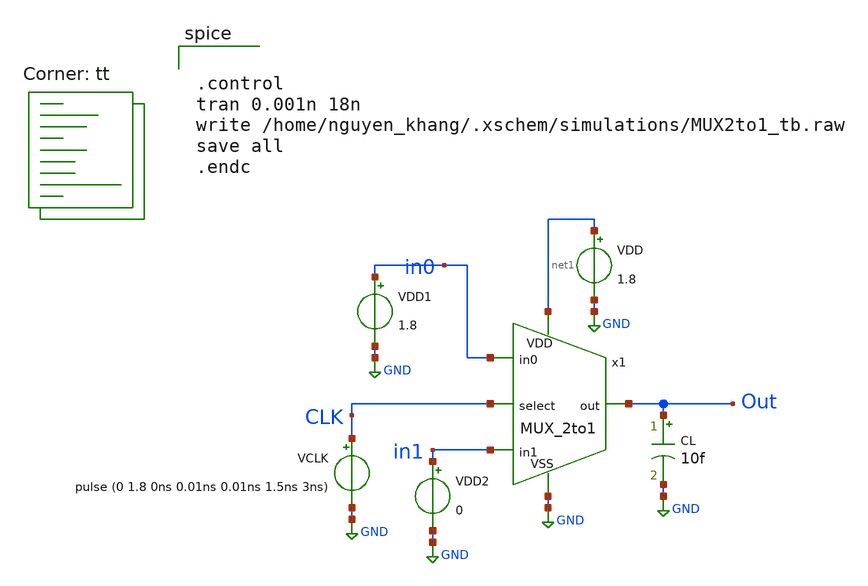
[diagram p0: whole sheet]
** sch_path: MUX_2to1_tb.sch
**.subckt MUX_2to1_tb
x1 in1 net1 Out CLK GND in0 MUX_2to1
VCLK CLK GND pulse (0 1.8 0ns 0.01ns 0.01ns 1.5ns 3ns)
VDD net1 GND 1.8
CL Out GND 10f m=1
VDD1 in0 GND 1.8
VDD2 in1 GND 0
**** begin user architecture code
.lib $::SKYWATER_MODELS/sky130.lib.spice tt


.control
tran 0.001n 18n
write /home/nguyen_khang/.xschem/simulations/MUX2to1_tb.raw
save all
.endc

**** end user architecture code
**.ends

* expanding   symbol:  project/MUX_2to1.sym # of pins=6
** sym_path: MUX_2to1.sym
** sch_path: MUX_2to1.sch
.subckt MUX_2to1 in1 VDD out select VSS in0
*.ipin select
*.ipin VSS
*.ipin VDD
*.ipin in1
*.ipin in0
*.opin out
XM1 net1 select VSS VSS sky130_fd_pr__nfet_01v8 L=0.15 W=1 nf=1 ad='int((nf+1)/2) * W/nf * 0.29' as='int((nf+2)/2) * W/nf * 0.29'
+ pd='2*int((nf+1)/2) * (W/nf + 0.29)' ps='2*int((nf+2)/2) * (W/nf + 0.29)' nrd='0.29 / W' nrs='0.29 / W'
+ sa=0 sb=0 sd=0 mult=1 m=1
XM2 net1 select VDD VDD sky130_fd_pr__pfet_01v8 L=0.15 W=2 nf=1 ad='int((nf+1)/2) * W/nf * 0.29' as='int((nf+2)/2) * W/nf * 0.29'
+ pd='2*int((nf+1)/2) * (W/nf + 0.29)' ps='2*int((nf+2)/2) * (W/nf + 0.29)' nrd='0.29 / W' nrs='0.29 / W'
+ sa=0 sb=0 sd=0 mult=1 m=1
XM3 out select in1 VSS sky130_fd_pr__nfet_01v8 L=0.15 W=3 nf=1 ad='int((nf+1)/2) * W/nf * 0.29' as='int((nf+2)/2) * W/nf * 0.29'
+ pd='2*int((nf+1)/2) * (W/nf + 0.29)' ps='2*int((nf+2)/2) * (W/nf + 0.29)' nrd='0.29 / W' nrs='0.29 / W'
+ sa=0 sb=0 sd=0 mult=1 m=1
XM4 out net1 in1 VDD sky130_fd_pr__pfet_01v8 L=0.15 W=3 nf=1 ad='int((nf+1)/2) * W/nf * 0.29' as='int((nf+2)/2) * W/nf * 0.29'
+ pd='2*int((nf+1)/2) * (W/nf + 0.29)' ps='2*int((nf+2)/2) * (W/nf + 0.29)' nrd='0.29 / W' nrs='0.29 / W'
+ sa=0 sb=0 sd=0 mult=1 m=1
XM5 out net1 in0 VSS sky130_fd_pr__nfet_01v8 L=0.15 W=3 nf=1 ad='int((nf+1)/2) * W/nf * 0.29' as='int((nf+2)/2) * W/nf * 0.29'
+ pd='2*int((nf+1)/2) * (W/nf + 0.29)' ps='2*int((nf+2)/2) * (W/nf + 0.29)' nrd='0.29 / W' nrs='0.29 / W'
+ sa=0 sb=0 sd=0 mult=1 m=1
XM6 out select in0 VDD sky130_fd_pr__pfet_01v8 L=0.15 W=3 nf=1 ad='int((nf+1)/2) * W/nf * 0.29' as='int((nf+2)/2) * W/nf * 0.29'
+ pd='2*int((nf+1)/2) * (W/nf + 0.29)' ps='2*int((nf+2)/2) * (W/nf + 0.29)' nrd='0.29 / W' nrs='0.29 / W'
+ sa=0 sb=0 sd=0 mult=1 m=1
.ends

.GLOBAL GND
.end
